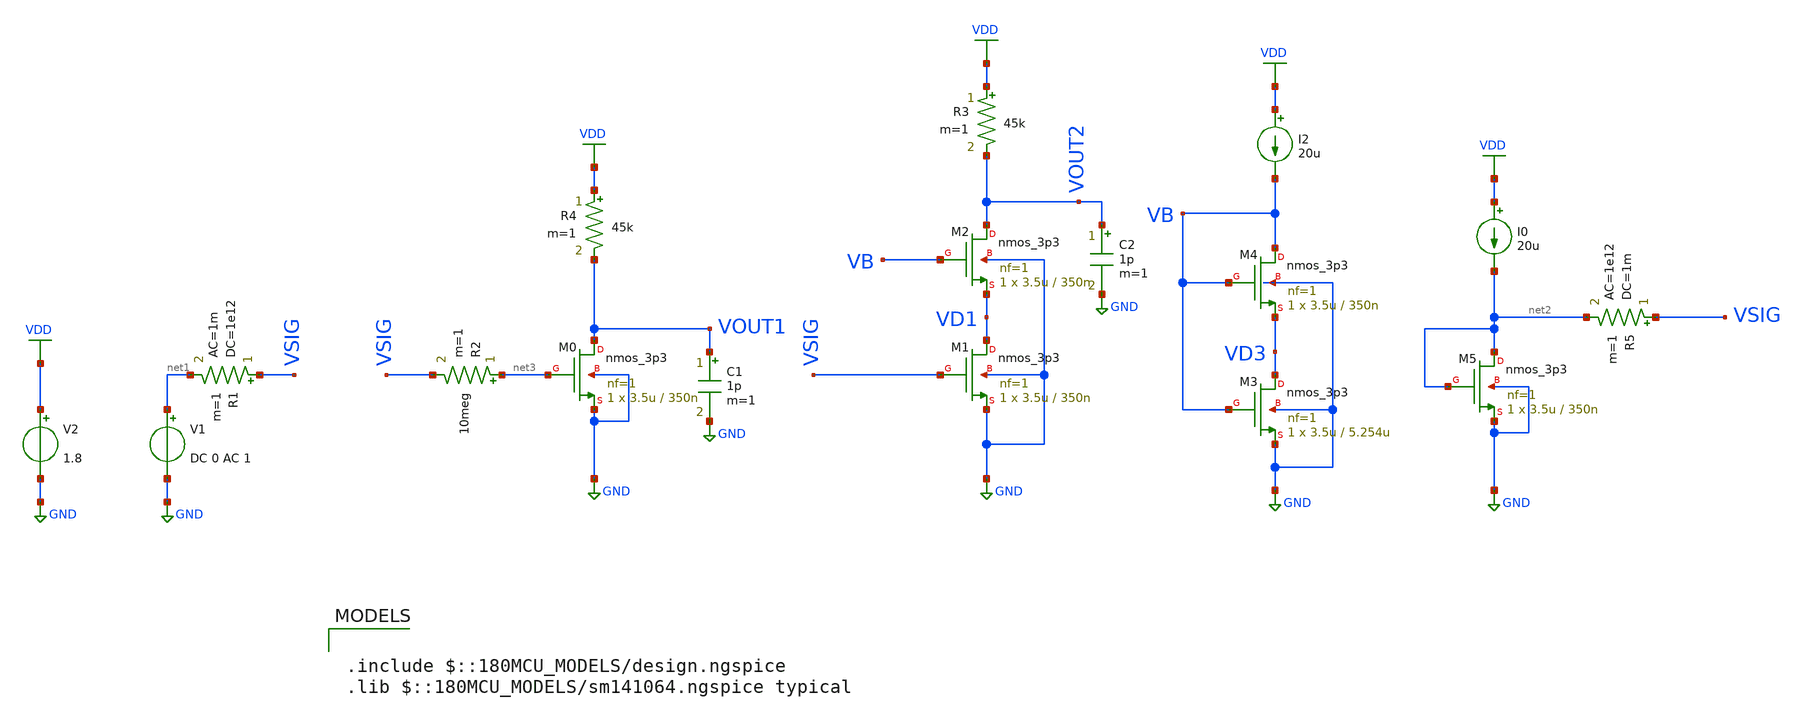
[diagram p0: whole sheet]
** sch_path: ITI_Labs/Lab3/Design/Lab03_bw.sch
**.subckt Lab03_bw
V1 net1 GND DC 0 AC 1
R1 VSIG net1 1e12 ac=1m m=1
XM0 VOUT1 net3 GND GND nmos_3p3 L=350n W=3.5u nf=1 ad='int((nf+1)/2) * W/nf * 0.18u' as='int((nf+2)/2) * W/nf * 0.18u'
+ pd='2*int((nf+1)/2) * (W/nf + 0.18u)' ps='2*int((nf+2)/2) * (W/nf + 0.18u)' nrd='0.18u / W' nrs='0.18u / W'
+ sa=0 sb=0 sd=0 m=1
C1 VOUT1 GND 1p m=1
V2 VDD GND 1.8
XM1 VD1 VSIG GND GND nmos_3p3 L=350n W=3.5u nf=1 ad='int((nf+1)/2) * W/nf * 0.18u' as='int((nf+2)/2) * W/nf * 0.18u'
+ pd='2*int((nf+1)/2) * (W/nf + 0.18u)' ps='2*int((nf+2)/2) * (W/nf + 0.18u)' nrd='0.18u / W' nrs='0.18u / W'
+ sa=0 sb=0 sd=0 m=1
XM2 VOUT2 VB VD1 GND nmos_3p3 L=350n W=3.5u nf=1 ad='int((nf+1)/2) * W/nf * 0.18u' as='int((nf+2)/2) * W/nf * 0.18u'
+ pd='2*int((nf+1)/2) * (W/nf + 0.18u)' ps='2*int((nf+2)/2) * (W/nf + 0.18u)' nrd='0.18u / W' nrs='0.18u / W'
+ sa=0 sb=0 sd=0 m=1
C2 VOUT2 GND 1p m=1
XM4 VB VB VD3 GND nmos_3p3 L=350n W=3.5u nf=1 ad='int((nf+1)/2) * W/nf * 0.18u' as='int((nf+2)/2) * W/nf * 0.18u'
+ pd='2*int((nf+1)/2) * (W/nf + 0.18u)' ps='2*int((nf+2)/2) * (W/nf + 0.18u)' nrd='0.18u / W' nrs='0.18u / W'
+ sa=0 sb=0 sd=0 m=1
I2 VDD VB 20u
XM3 VD3 VB GND GND nmos_3p3 L=5.254u W=3.5u nf=1 ad='int((nf+1)/2) * W/nf * 0.18u' as='int((nf+2)/2) * W/nf * 0.18u'
+ pd='2*int((nf+1)/2) * (W/nf + 0.18u)' ps='2*int((nf+2)/2) * (W/nf + 0.18u)' nrd='0.18u / W' nrs='0.18u / W'
+ sa=0 sb=0 sd=0 m=1
R4 VDD VOUT1 45k m=1
R3 VDD VOUT2 45k m=1
XM5 net2 net2 GND GND nmos_3p3 L=350n W=3.5u nf=1 ad='int((nf+1)/2) * W/nf * 0.18u' as='int((nf+2)/2) * W/nf * 0.18u'
+ pd='2*int((nf+1)/2) * (W/nf + 0.18u)' ps='2*int((nf+2)/2) * (W/nf + 0.18u)' nrd='0.18u / W' nrs='0.18u / W'
+ sa=0 sb=0 sd=0 m=1
I0 VDD net2 20u
R5 VSIG net2 1m ac=1e12 m=1
R2 net3 VSIG 10meg m=1
**** begin user architecture code

.include $::180MCU_MODELS/design.ngspice
.lib $::180MCU_MODELS/sm141064.ngspice typical



.include sim_script.sim


**** end user architecture code
**.ends
.GLOBAL GND
.GLOBAL VDD
.end
